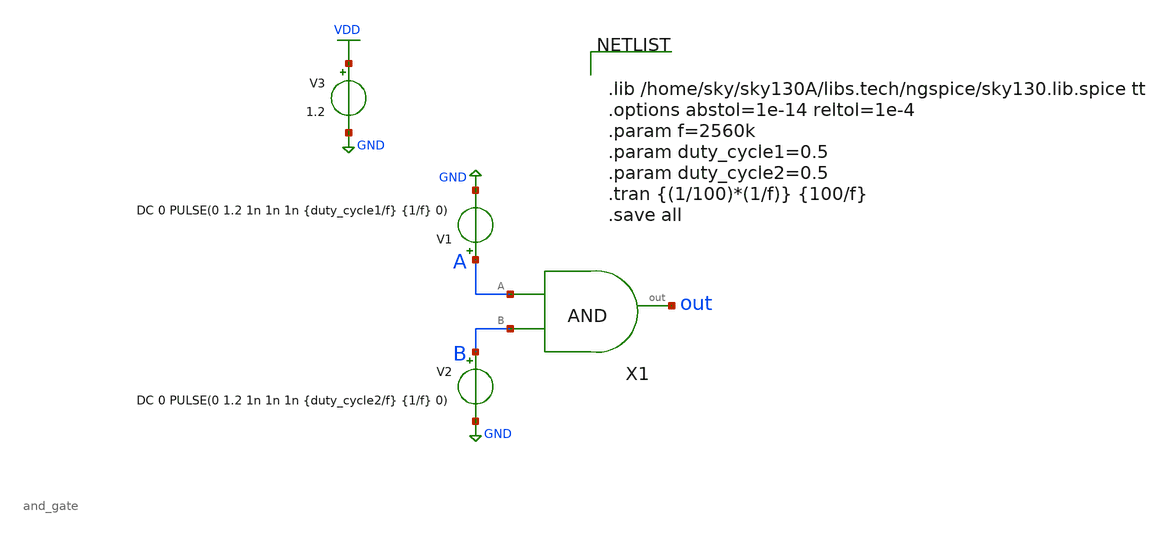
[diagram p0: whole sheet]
** sch_path: xschem/and_gate/and_gate_tb.sch
**.subckt and_gate_tb
X1 A B out and_gate
V1 A GND DC 0 PULSE(0 1.2 1n 1n 1n {duty_cycle1/f} {1/f} 0)
V2 B GND DC 0 PULSE(0 1.2 1n 1n 1n {duty_cycle2/f} {1/f} 0)
V3 VDD GND 1.2
**** begin user architecture code


.lib /home/sky/sky130A/libs.tech/ngspice/sky130.lib.spice tt
.options abstol=1e-14 reltol=1e-4
.param f=2560k
.param duty_cycle1=0.5
.param duty_cycle2=0.5
.tran {(1/100)*(1/f)} {100/f}
.save all


**** end user architecture code
**.ends

* expanding   symbol:  and_gate/and_gate.sym # of pins=3
** sym_path: xschem/and_gate/and_gate.sym
** sch_path: xschem/and_gate/and_gate.sch
.subckt and_gate A B out
*.ipin A
*.ipin B
*.opin out
XM1 net1 A net2 GND sky130_fd_pr__nfet_01v8 L=0.18 W=1 nf=1 ad='int((nf+1)/2) * W/nf * 0.29' as='int((nf+2)/2) * W/nf * 0.29'
+ pd='2*int((nf+1)/2) * (W/nf + 0.29)' ps='2*int((nf+2)/2) * (W/nf + 0.29)' nrd='0.29 / W' nrs='0.29 / W'
+ sa=0 sb=0 sd=0 mult=1 m=1
XM2 net1 A VDD VDD sky130_fd_pr__pfet_01v8 L=0.18 W=1 nf=1 ad='int((nf+1)/2) * W/nf * 0.29' as='int((nf+2)/2) * W/nf * 0.29'
+ pd='2*int((nf+1)/2) * (W/nf + 0.29)' ps='2*int((nf+2)/2) * (W/nf + 0.29)' nrd='0.29 / W' nrs='0.29 / W'
+ sa=0 sb=0 sd=0 mult=1 m=1
XM3 net1 B VDD VDD sky130_fd_pr__pfet_01v8 L=0.18 W=1 nf=1 ad='int((nf+1)/2) * W/nf * 0.29' as='int((nf+2)/2) * W/nf * 0.29'
+ pd='2*int((nf+1)/2) * (W/nf + 0.29)' ps='2*int((nf+2)/2) * (W/nf + 0.29)' nrd='0.29 / W' nrs='0.29 / W'
+ sa=0 sb=0 sd=0 mult=1 m=1
XM4 net2 B GND GND sky130_fd_pr__nfet_01v8 L=0.18 W=1 nf=1 ad='int((nf+1)/2) * W/nf * 0.29' as='int((nf+2)/2) * W/nf * 0.29'
+ pd='2*int((nf+1)/2) * (W/nf + 0.29)' ps='2*int((nf+2)/2) * (W/nf + 0.29)' nrd='0.29 / W' nrs='0.29 / W'
+ sa=0 sb=0 sd=0 mult=1 m=1
X1 net1 out inv Wpmos=3 Lpmos=0.18 Wnmos=1 Lnmos=0.18
.ends


* expanding   symbol:  inv/inv.sym # of pins=2
** sym_path: xschem/inv/inv.sym
** sch_path: xschem/inv/inv.sch
.subckt inv in out  Wpmos=3 Lpmos=0.18 Wnmos=1 Lnmos=0.18
*.ipin in
*.iopin out
XM1 out in GND GND sky130_fd_pr__nfet_01v8 L=Lnmos W=Wnmos nf=1 ad='int((nf+1)/2) * W/nf * 0.29' as='int((nf+2)/2) * W/nf * 0.29'
+ pd='2*int((nf+1)/2) * (W/nf + 0.29)' ps='2*int((nf+2)/2) * (W/nf + 0.29)' nrd='0.29 / W' nrs='0.29 / W'
+ sa=0 sb=0 sd=0 mult=1 m=1
XM2 out in VDD VDD sky130_fd_pr__pfet_01v8 L=Lpmos W=Wpmos nf=1 ad='int((nf+1)/2) * W/nf * 0.29' as='int((nf+2)/2) * W/nf * 0.29'
+ pd='2*int((nf+1)/2) * (W/nf + 0.29)' ps='2*int((nf+2)/2) * (W/nf + 0.29)' nrd='0.29 / W' nrs='0.29 / W'
+ sa=0 sb=0 sd=0 mult=1 m=1
.ends

.GLOBAL GND
.GLOBAL VDD
.end
